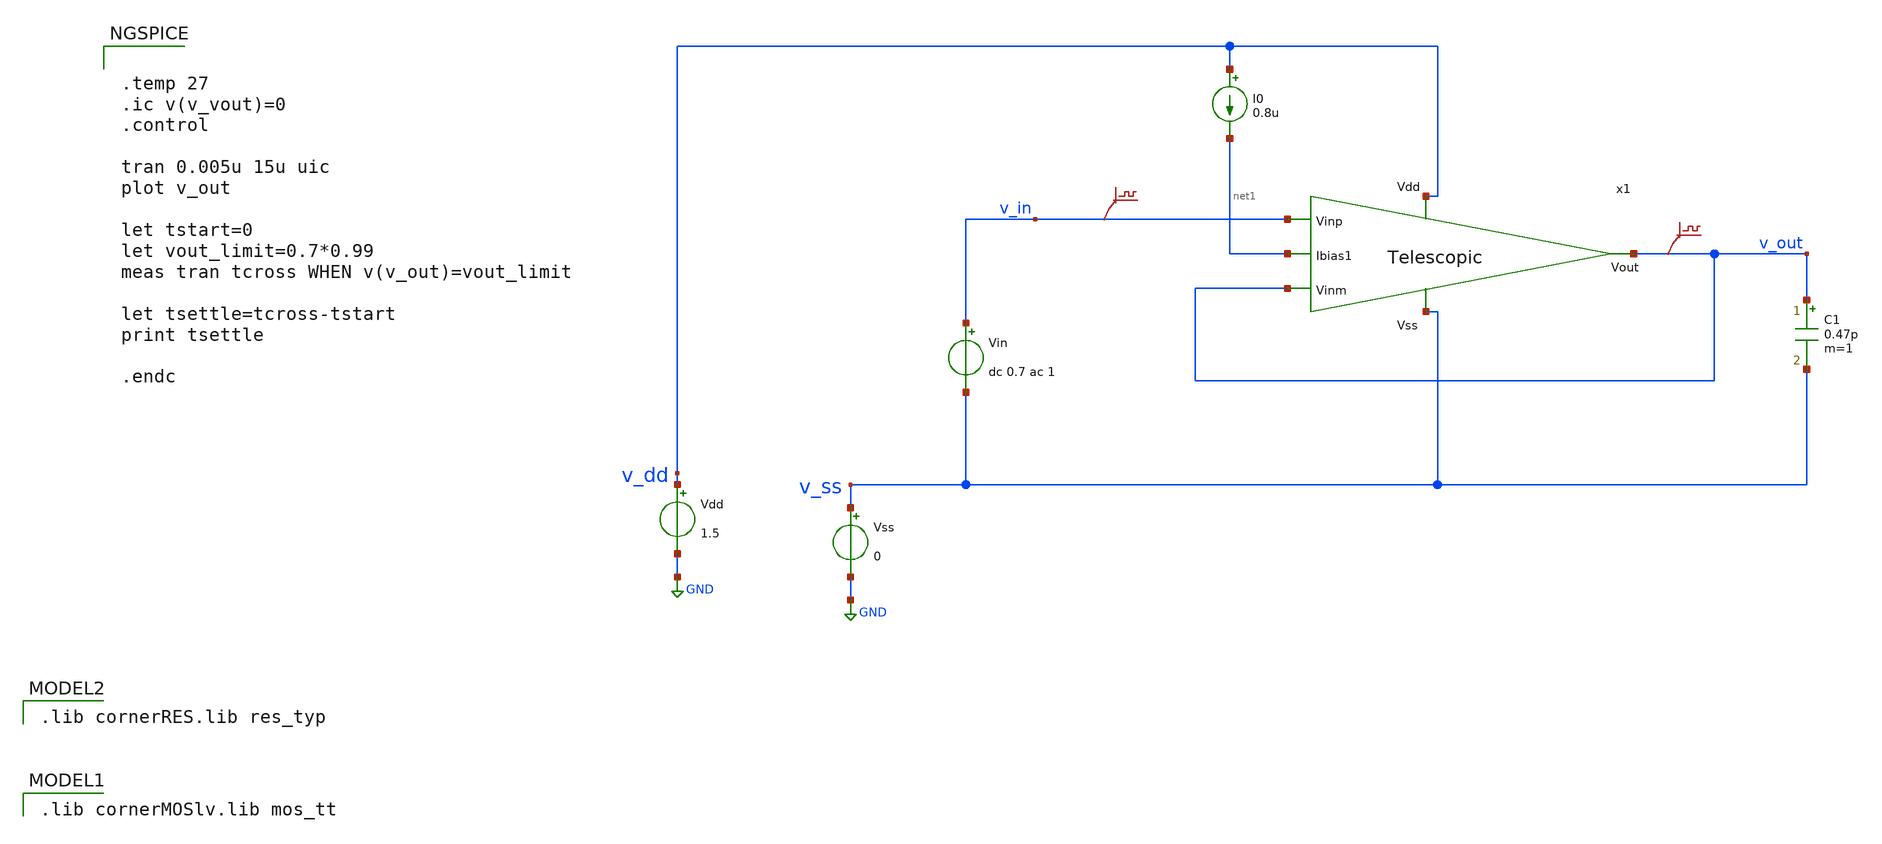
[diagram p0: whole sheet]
** sch_path: zip_meiners/ic_design/design_switch_cap/tb_Telescopic_tran.sch
* (c) 2024 Priyanka, @HSB
**.subckt tb_Telescopic_tran
Vss v_ss GND 0
Vdd v_dd GND 1.5
Vin v_in v_ss dc 0.7 ac 1
.save v(v_in)
I0 v_dd net1 0.8u
C1 v_out v_ss 0.47p m=1
.save v(v_out)
x1 v_dd net1 v_out v_out v_in v_ss Telescopic
**** begin user architecture code
 .lib cornerMOSlv.lib mos_tt

 .lib cornerRES.lib res_typ



.temp 27
.ic v(v_vout)=0
.control

tran 0.005u 15u uic
plot v_out

let tstart=0
let vout_limit=0.7*0.99
meas tran tcross WHEN v(v_out)=vout_limit

let tsettle=tcross-tstart
print tsettle

.endc


**** end user architecture code
**.ends

* expanding   symbol:  Telescopic.sym # of pins=6
** sym_path: Telescopic.sym
** sch_path: Telescopic.sch
.subckt Telescopic Vdd Ibias1 Vout Vinm Vinp Vss
*.ipin Vinp
*.opin Vout
*.ipin Vinm
*.ipin Vss
*.ipin Vdd
*.ipin Ibias1
XM19 net1 net7 Vss Vss sg13_lv_nmos w=0.3u l=2u ng=1 m=1 mm_ok=1
XM11 net2 Vinp net1 Vss sg13_lv_nmos w=0.15u l=2u ng=1 m=1 mm_ok=1
XM14 net3 Vinm net1 Vss sg13_lv_nmos w=0.15u l=2u ng=1 m=1 mm_ok=1
XM20 Vout net5 net4 Vdd sg13_lv_pmos w=0.16u l=0.5u ng=1 m=1 mm_ok=1
XM25 net9 net5 net10 Vdd sg13_lv_pmos w=0.16u l=0.5u ng=1 m=1 mm_ok=1
XM1 net5 net7 Vss Vss sg13_lv_nmos w=0.15u l=2u ng=1 m=1 mm_ok=1
XM2 net8 net7 Vss Vss sg13_lv_nmos w=0.15u l=2u ng=1 m=1 mm_ok=1
XM3 Vdd Ibias1 net8 Vss sg13_lv_nmos w=0.15u l=2u ng=1 m=1 mm_ok=1
XM4 Vout Ibias1 net3 Vss sg13_lv_nmos w=0.15u l=2u ng=1 m=1 mm_ok=1
XM5 net9 Ibias1 net2 Vss sg13_lv_nmos w=0.15u l=2u ng=1 m=1 mm_ok=1
XM6 net4 net6 Vdd Vdd sg13_lv_pmos w=0.16u l=0.5u ng=1 m=1 mm_ok=1
XM7 net6 net6 Vdd Vdd sg13_lv_pmos w=0.16u l=0.5u ng=1 m=1 mm_ok=1
XM8 net5 net5 net6 Vdd sg13_lv_pmos w=0.16u l=0.5u ng=1 m=1 mm_ok=1
XM9 net10 net6 Vdd Vdd sg13_lv_pmos w=0.16u l=0.5u ng=1 m=1 mm_ok=1
XM10 net7 net7 Vss Vss sg13_lv_nmos w=0.15u l=2u ng=1 m=1 mm_ok=1
XM12 Ibias1 Ibias1 net7 Vss sg13_lv_nmos w=0.15u l=2u ng=1 m=1 mm_ok=1
.ends

.GLOBAL GND
.end
